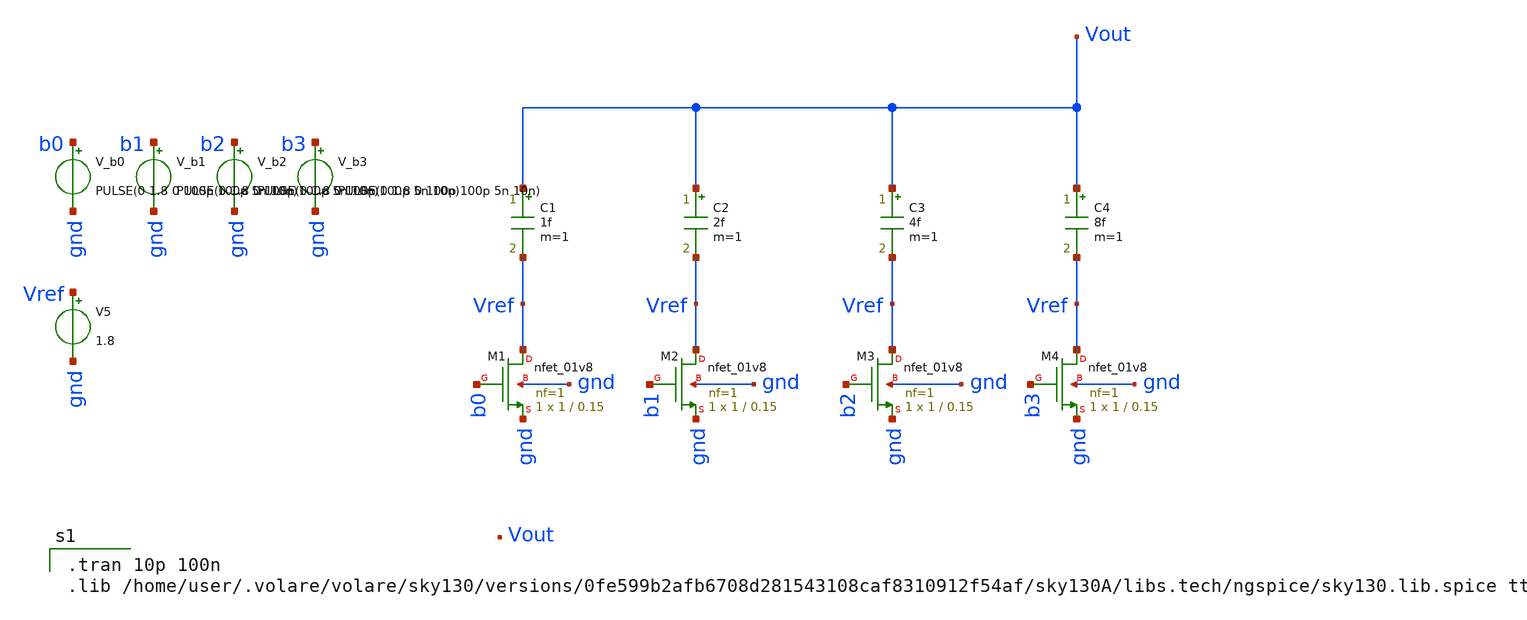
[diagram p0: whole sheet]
** sch_path: sar_adc_dac_monotonic/untitled-1.sch
**.subckt untitled-1
XM1 Vref b0 gnd gnd sky130_fd_pr__nfet_01v8 L=0.15 W=1 nf=1 ad='int((nf+1)/2) * W/nf * 0.29' as='int((nf+2)/2) * W/nf * 0.29'
+ pd='2*int((nf+1)/2) * (W/nf + 0.29)' ps='2*int((nf+2)/2) * (W/nf + 0.29)' nrd='0.29 / W' nrs='0.29 / W'
+ sa=0 sb=0 sd=0 mult=1 m=1
XM2 Vref b1 gnd gnd sky130_fd_pr__nfet_01v8 L=0.15 W=1 nf=1 ad='int((nf+1)/2) * W/nf * 0.29' as='int((nf+2)/2) * W/nf * 0.29'
+ pd='2*int((nf+1)/2) * (W/nf + 0.29)' ps='2*int((nf+2)/2) * (W/nf + 0.29)' nrd='0.29 / W' nrs='0.29 / W'
+ sa=0 sb=0 sd=0 mult=1 m=1
XM3 Vref b2 gnd gnd sky130_fd_pr__nfet_01v8 L=0.15 W=1 nf=1 ad='int((nf+1)/2) * W/nf * 0.29' as='int((nf+2)/2) * W/nf * 0.29'
+ pd='2*int((nf+1)/2) * (W/nf + 0.29)' ps='2*int((nf+2)/2) * (W/nf + 0.29)' nrd='0.29 / W' nrs='0.29 / W'
+ sa=0 sb=0 sd=0 mult=1 m=1
XM4 Vref b3 gnd gnd sky130_fd_pr__nfet_01v8 L=0.15 W=1 nf=1 ad='int((nf+1)/2) * W/nf * 0.29' as='int((nf+2)/2) * W/nf * 0.29'
+ pd='2*int((nf+1)/2) * (W/nf + 0.29)' ps='2*int((nf+2)/2) * (W/nf + 0.29)' nrd='0.29 / W' nrs='0.29 / W'
+ sa=0 sb=0 sd=0 mult=1 m=1
C1 Vout Vref 1f m=1
C2 Vout Vref 2f m=1
C3 Vout Vref 4f m=1
C4 Vout Vref 8f m=1
V_b0 b0 gnd PULSE(0 1.8 0 100p 100p 5n 10n)
V_b1 b1 gnd PULSE(0 1.8 0 100p 100p 5n 10n)
V_b2 b2 gnd PULSE(0 1.8 0 100p 100p 5n 10n)
V_b3 b3 gnd PULSE(0 1.8 0 100p 100p 5n 10n)
V5 Vref gnd 1.8
**** begin user architecture code

.tran 10p 100n
.lib /home/user/.volare/volare/sky130/versions/0fe599b2afb6708d281543108caf8310912f54af/sky130A/libs.tech/ngspice/sky130.lib.spice tt

**** end user architecture code
**.ends
.end
